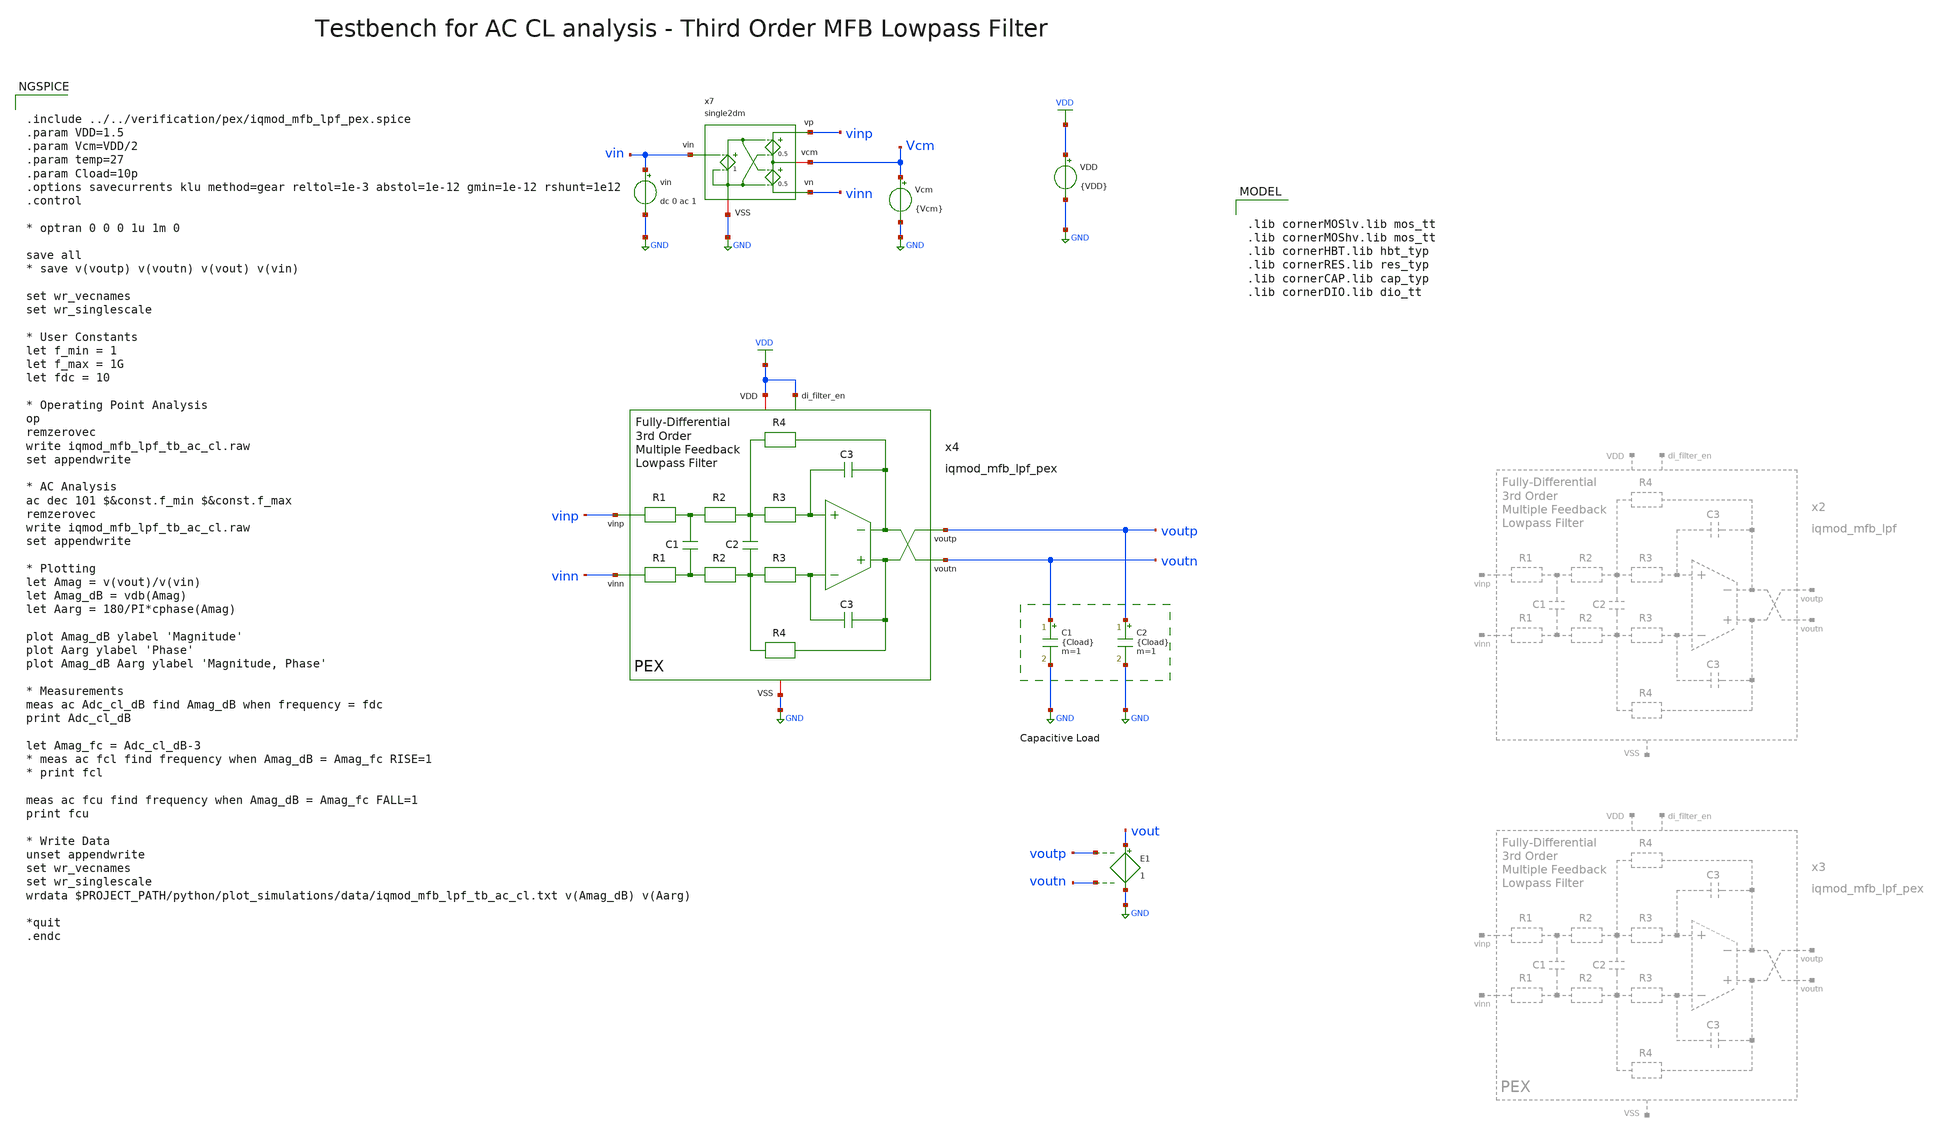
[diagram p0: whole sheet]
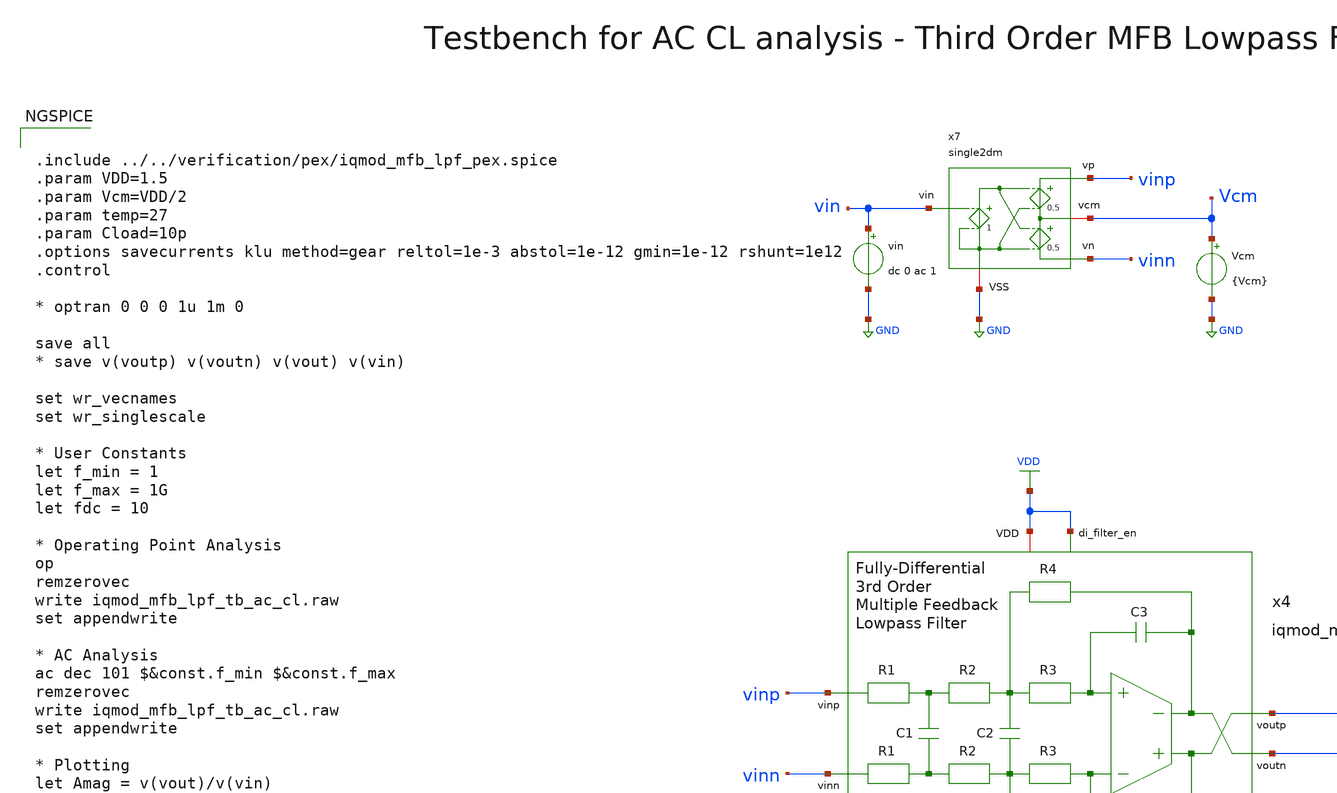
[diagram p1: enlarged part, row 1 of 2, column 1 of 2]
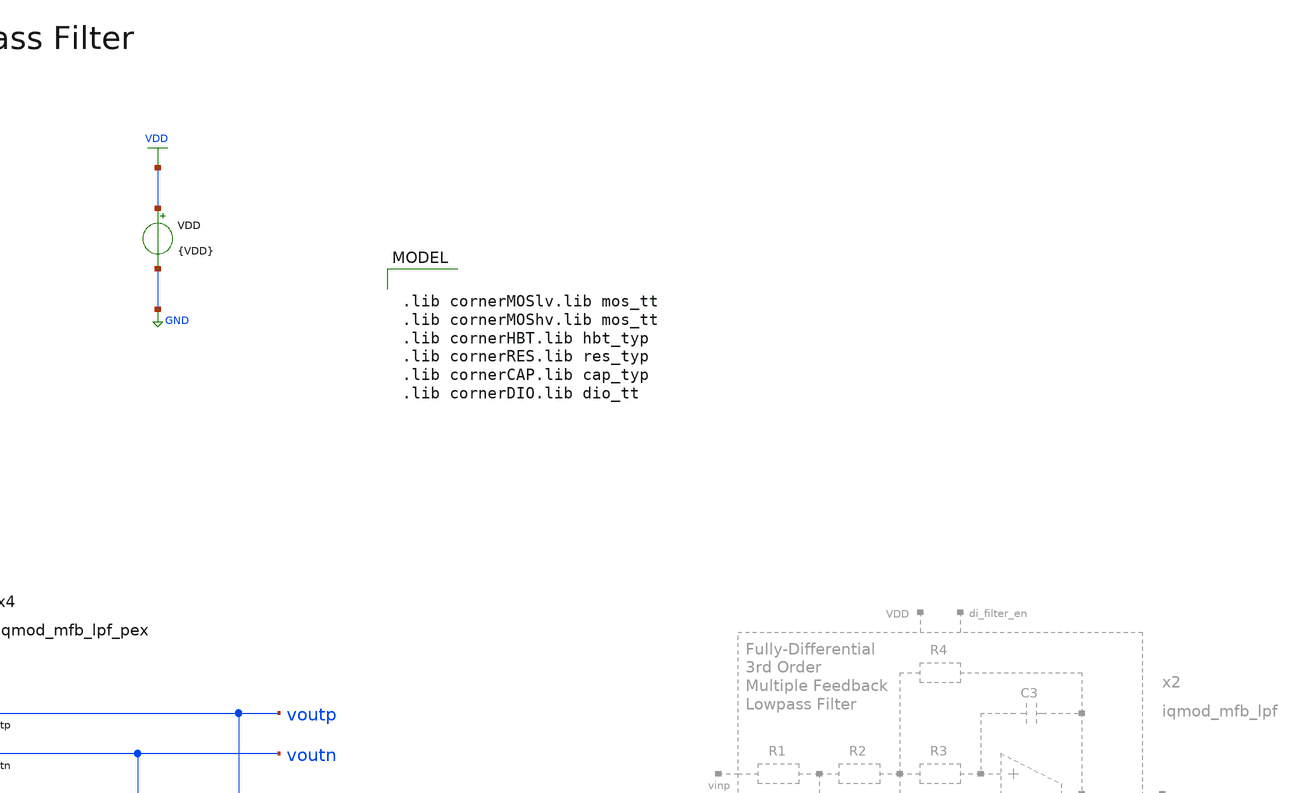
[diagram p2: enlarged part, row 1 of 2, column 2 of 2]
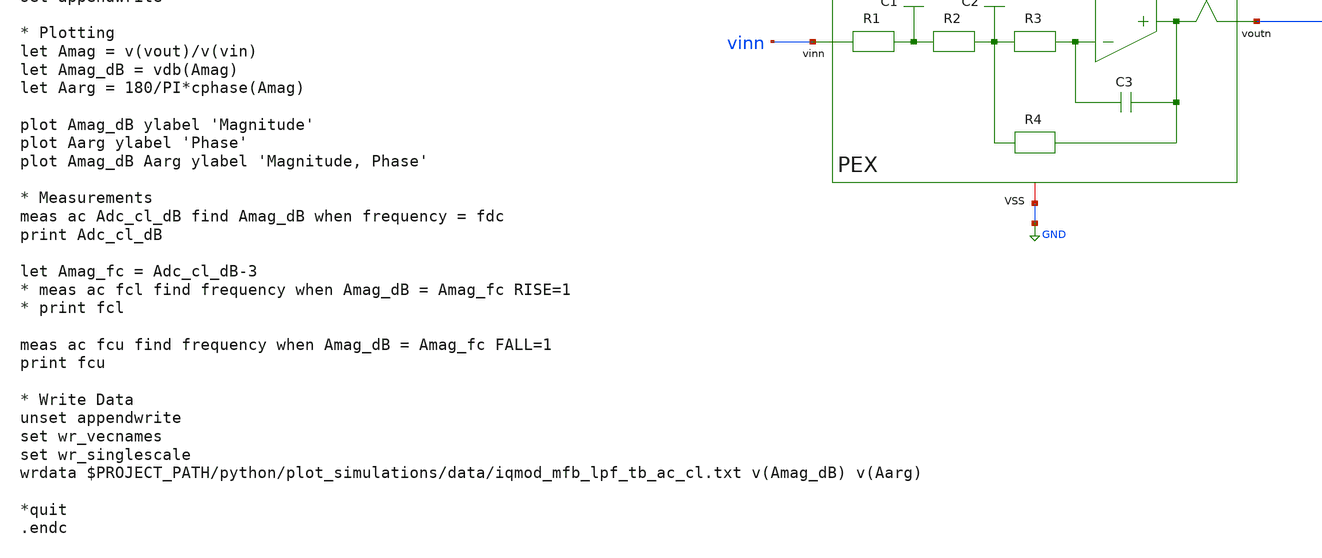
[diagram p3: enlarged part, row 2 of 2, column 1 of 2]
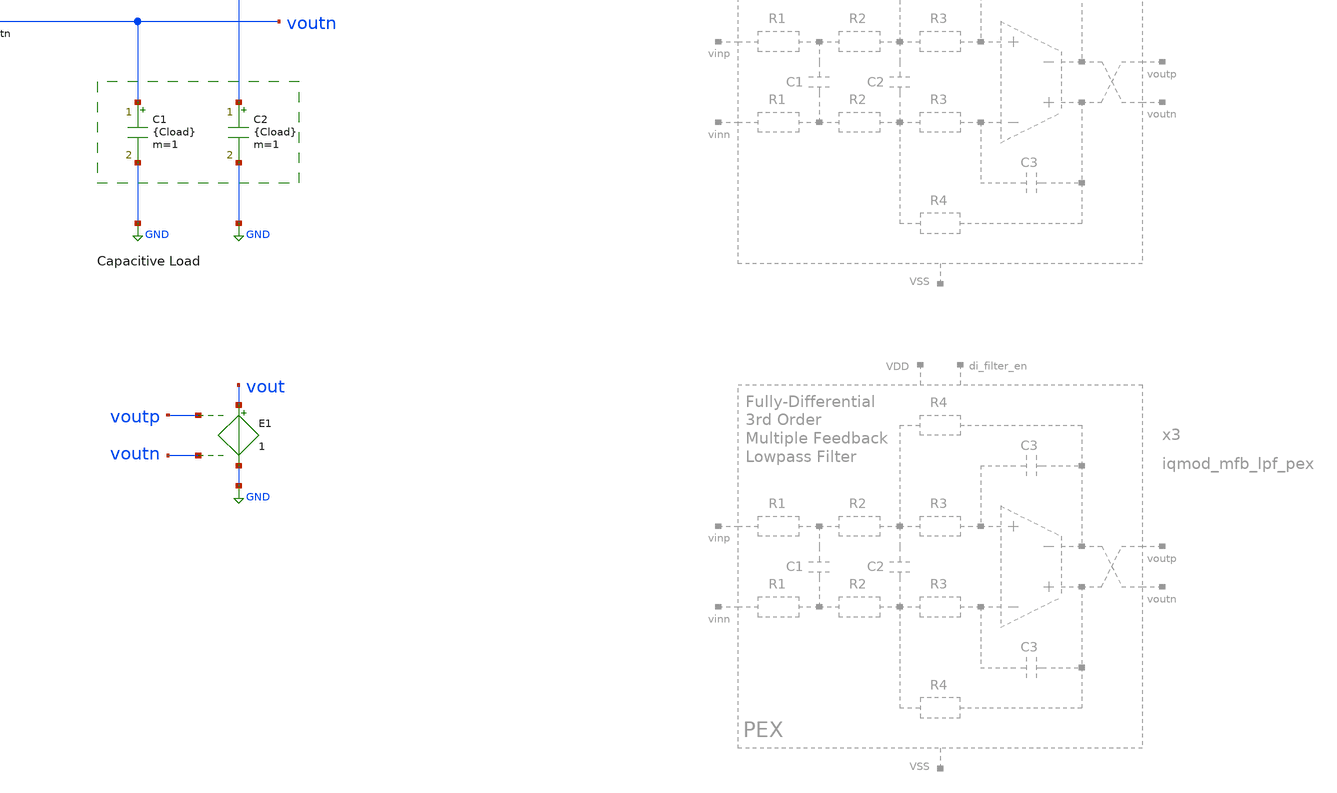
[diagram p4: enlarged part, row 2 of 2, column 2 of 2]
** sch_path: ihp130/macros/iqmod/xschem/testbenches/iqmod_mfb_lpf_tb_ac_cl.sch
**.subckt iqmod_mfb_lpf_tb_ac_cl
VDD VDD GND {VDD}
C1 voutn GND {Cload} m=1
C2 voutp GND {Cload} m=1
E1 vout GND voutp voutn 1
Vcm Vcm GND {Vcm}
vin vin GND dc 0 ac 1
x7 vinp vin Vcm GND vinn single2dm
x4 voutp vinp voutn vinn VDD GND VDD iqmod_mfb_lpf_pex
**** begin user architecture code


.include ../../verification/pex/iqmod_mfb_lpf_pex.spice
.param VDD=1.5
.param Vcm=VDD/2
.param temp=27
.param Cload=10p
.options savecurrents klu method=gear reltol=1e-3 abstol=1e-12 gmin=1e-12 rshunt=1e12
.control

* optran 0 0 0 1u 1m 0

save all
* save v(voutp) v(voutn) v(vout) v(vin)

set wr_vecnames
set wr_singlescale

* User Constants
let f_min = 1
let f_max = 1G
let fdc = 10

* Operating Point Analysis
op
remzerovec
write iqmod_mfb_lpf_tb_ac_cl.raw
set appendwrite

* AC Analysis
ac dec 101 $&const.f_min $&const.f_max
remzerovec
write iqmod_mfb_lpf_tb_ac_cl.raw
set appendwrite

* Plotting
let Amag = v(vout)/v(vin)
let Amag_dB = vdb(Amag)
let Aarg = 180/PI*cphase(Amag)

plot Amag_dB ylabel 'Magnitude'
plot Aarg ylabel 'Phase'
plot Amag_dB Aarg ylabel 'Magnitude, Phase'

* Measurements
meas ac Adc_cl_dB find Amag_dB when frequency = fdc
print Adc_cl_dB

let Amag_fc = Adc_cl_dB-3
* meas ac fcl find frequency when Amag_dB = Amag_fc RISE=1
* print fcl

meas ac fcu find frequency when Amag_dB = Amag_fc FALL=1
print fcu

* Write Data
unset appendwrite
set wr_vecnames
set wr_singlescale
wrdata $PROJECT_PATH/python/plot_simulations/data/iqmod_mfb_lpf_tb_ac_cl.txt v(Amag_dB) v(Aarg)

*quit
.endc



.lib cornerMOSlv.lib mos_tt
.lib cornerMOShv.lib mos_tt
.lib cornerHBT.lib hbt_typ
.lib cornerRES.lib res_typ
.lib cornerCAP.lib cap_typ
.lib cornerDIO.lib dio_tt

**** end user architecture code
**.ends
.GLOBAL GND
.GLOBAL VDD
.end
